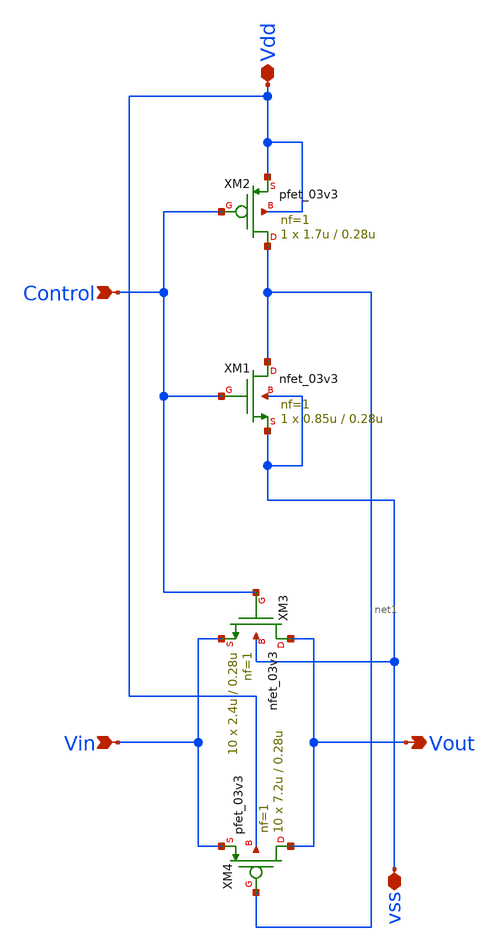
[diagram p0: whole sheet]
** sch_path: designs/libs/core_analog/Transmission_Gate/transmission_gate_1.sch
**.subckt transmission_gate_1 Vdd Control Vout Vin vss
*.iopin Vdd
*.ipin Control
*.opin Vout
*.ipin Vin
*.iopin vss
XM1 net1 Control vss vss nfet_03v3 L=0.28u W=0.85u nf=1 ad='int((nf+1)/2) * W/nf * 0.18u' as='int((nf+2)/2) * W/nf * 0.18u'
+ pd='2*int((nf+1)/2) * (W/nf + 0.18u)' ps='2*int((nf+2)/2) * (W/nf + 0.18u)' nrd='0.18u / W' nrs='0.18u / W'
+ sa=0 sb=0 sd=0 m=1
XM2 net1 Control Vdd Vdd pfet_03v3 L=0.28u W=1.7u nf=1 ad='int((nf+1)/2) * W/nf * 0.18u' as='int((nf+2)/2) * W/nf * 0.18u'
+ pd='2*int((nf+1)/2) * (W/nf + 0.18u)' ps='2*int((nf+2)/2) * (W/nf + 0.18u)' nrd='0.18u / W' nrs='0.18u / W'
+ sa=0 sb=0 sd=0 m=1
XM3 Vout Control Vin vss nfet_03v3 L=0.28u W=2.4u nf=1 ad='int((nf+1)/2) * W/nf * 0.18u' as='int((nf+2)/2) * W/nf * 0.18u'
+ pd='2*int((nf+1)/2) * (W/nf + 0.18u)' ps='2*int((nf+2)/2) * (W/nf + 0.18u)' nrd='0.18u / W' nrs='0.18u / W'
+ sa=0 sb=0 sd=0 m=10
XM4 Vout net1 Vin Vdd pfet_03v3 L=0.28u W=7.2u nf=1 ad='int((nf+1)/2) * W/nf * 0.18u' as='int((nf+2)/2) * W/nf * 0.18u'
+ pd='2*int((nf+1)/2) * (W/nf + 0.18u)' ps='2*int((nf+2)/2) * (W/nf + 0.18u)' nrd='0.18u / W' nrs='0.18u / W'
+ sa=0 sb=0 sd=0 m=10
**.ends
.end
